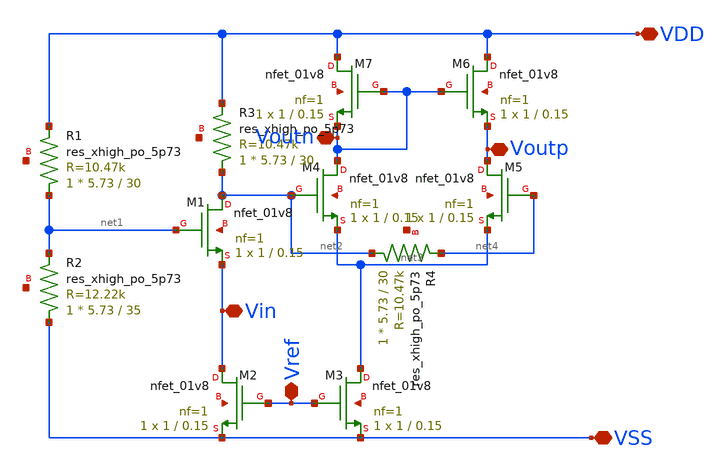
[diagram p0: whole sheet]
** sch_path: hw06/xschem/untitled.sch
**.subckt untitled VSS VDD Voutp Voutn Vref Vin
*.iopin VSS
*.iopin VDD
*.iopin Voutp
*.iopin Voutn
*.iopin Vref
*.iopin Vin
XR1 net1 VDD net5 sky130_fd_pr__res_xhigh_po_5p73 L=30 mult=1 m=1
XR2 VSS net1 net6 sky130_fd_pr__res_xhigh_po_5p73 L=35 mult=1 m=1
XM1 net2 net1 Vin net7 sky130_fd_pr__nfet_01v8 L=0.15 W=1 nf=1 ad='int((nf+1)/2) * W/nf * 0.29' as='int((nf+2)/2) * W/nf * 0.29'
+ pd='2*int((nf+1)/2) * (W/nf + 0.29)' ps='2*int((nf+2)/2) * (W/nf + 0.29)' nrd='0.29 / W' nrs='0.29 / W'
+ sa=0 sb=0 sd=0 mult=1 m=1
XM2 Vin Vref VSS net8 sky130_fd_pr__nfet_01v8 L=0.15 W=1 nf=1 ad='int((nf+1)/2) * W/nf * 0.29' as='int((nf+2)/2) * W/nf * 0.29'
+ pd='2*int((nf+1)/2) * (W/nf + 0.29)' ps='2*int((nf+2)/2) * (W/nf + 0.29)' nrd='0.29 / W' nrs='0.29 / W'
+ sa=0 sb=0 sd=0 mult=1 m=1
XM3 net3 Vref VSS net9 sky130_fd_pr__nfet_01v8 L=0.15 W=1 nf=1 ad='int((nf+1)/2) * W/nf * 0.29' as='int((nf+2)/2) * W/nf * 0.29'
+ pd='2*int((nf+1)/2) * (W/nf + 0.29)' ps='2*int((nf+2)/2) * (W/nf + 0.29)' nrd='0.29 / W' nrs='0.29 / W'
+ sa=0 sb=0 sd=0 mult=1 m=1
XM4 Voutn net2 net3 net10 sky130_fd_pr__nfet_01v8 L=0.15 W=1 nf=1 ad='int((nf+1)/2) * W/nf * 0.29' as='int((nf+2)/2) * W/nf * 0.29'
+ pd='2*int((nf+1)/2) * (W/nf + 0.29)' ps='2*int((nf+2)/2) * (W/nf + 0.29)' nrd='0.29 / W' nrs='0.29 / W'
+ sa=0 sb=0 sd=0 mult=1 m=1
XM5 Voutp net4 net3 net11 sky130_fd_pr__nfet_01v8 L=0.15 W=1 nf=1 ad='int((nf+1)/2) * W/nf * 0.29' as='int((nf+2)/2) * W/nf * 0.29'
+ pd='2*int((nf+1)/2) * (W/nf + 0.29)' ps='2*int((nf+2)/2) * (W/nf + 0.29)' nrd='0.29 / W' nrs='0.29 / W'
+ sa=0 sb=0 sd=0 mult=1 m=1
XM6 VDD Voutn Voutp net12 sky130_fd_pr__nfet_01v8 L=0.15 W=1 nf=1 ad='int((nf+1)/2) * W/nf * 0.29' as='int((nf+2)/2) * W/nf * 0.29'
+ pd='2*int((nf+1)/2) * (W/nf + 0.29)' ps='2*int((nf+2)/2) * (W/nf + 0.29)' nrd='0.29 / W' nrs='0.29 / W'
+ sa=0 sb=0 sd=0 mult=1 m=1
XM7 VDD Voutn Voutn net13 sky130_fd_pr__nfet_01v8 L=0.15 W=1 nf=1 ad='int((nf+1)/2) * W/nf * 0.29' as='int((nf+2)/2) * W/nf * 0.29'
+ pd='2*int((nf+1)/2) * (W/nf + 0.29)' ps='2*int((nf+2)/2) * (W/nf + 0.29)' nrd='0.29 / W' nrs='0.29 / W'
+ sa=0 sb=0 sd=0 mult=1 m=1
XR3 net2 VDD net14 sky130_fd_pr__res_xhigh_po_5p73 L=30 mult=1 m=1
XR4 net2 net4 net15 sky130_fd_pr__res_xhigh_po_5p73 L=30 mult=1 m=1
**.ends
.end
